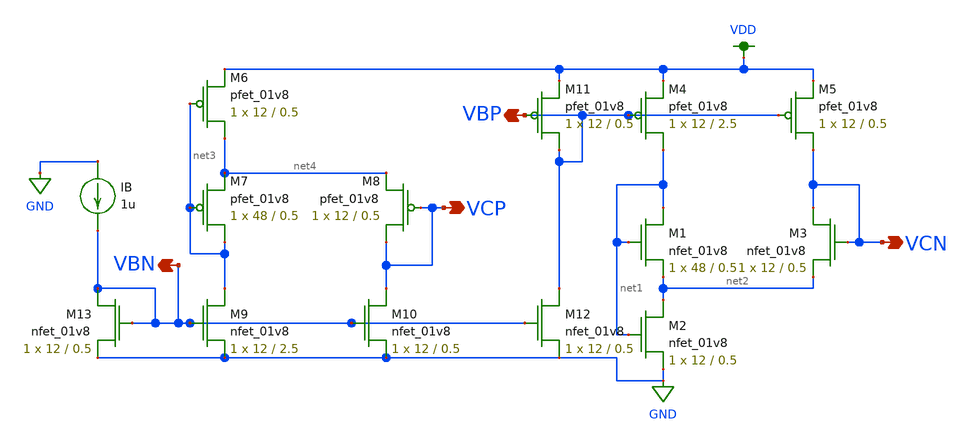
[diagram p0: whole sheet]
** sch_path: MP3/BiasGen (copy).sch
**.subckt BiasGen (copy) VCN VCP VBP VBN
*.opin VCN
*.opin VCP
*.opin VBP
*.opin VBN
XM1 net1 net1 net2 GND sky130_fd_pr__nfet_01v8 L=0.5 W=48 nf=1 ad='int((nf+1)/2) * W/nf * 0.29' as='int((nf+2)/2) * W/nf * 0.29'
+ pd='2*int((nf+1)/2) * (W/nf + 0.29)' ps='2*int((nf+2)/2) * (W/nf + 0.29)' nrd='0.29 / W' nrs='0.29 / W'
+ sa=0 sb=0 sd=0 mult=1 m=1
XM2 net2 net1 GND GND sky130_fd_pr__nfet_01v8 L=0.5 W=12 nf=1 ad='int((nf+1)/2) * W/nf * 0.29' as='int((nf+2)/2) * W/nf * 0.29'
+ pd='2*int((nf+1)/2) * (W/nf + 0.29)' ps='2*int((nf+2)/2) * (W/nf + 0.29)' nrd='0.29 / W' nrs='0.29 / W'
+ sa=0 sb=0 sd=0 mult=1 m=1
XM3 VCN VCN net2 GND sky130_fd_pr__nfet_01v8 L=0.5 W=12 nf=1 ad='int((nf+1)/2) * W/nf * 0.29' as='int((nf+2)/2) * W/nf * 0.29'
+ pd='2*int((nf+1)/2) * (W/nf + 0.29)' ps='2*int((nf+2)/2) * (W/nf + 0.29)' nrd='0.29 / W' nrs='0.29 / W'
+ sa=0 sb=0 sd=0 mult=1 m=1
XM4 net1 VBP VDD VDD sky130_fd_pr__pfet_01v8 L=2.5 W=12 nf=1 ad='int((nf+1)/2) * W/nf * 0.29' as='int((nf+2)/2) * W/nf * 0.29'
+ pd='2*int((nf+1)/2) * (W/nf + 0.29)' ps='2*int((nf+2)/2) * (W/nf + 0.29)' nrd='0.29 / W' nrs='0.29 / W'
+ sa=0 sb=0 sd=0 mult=1 m=1
XM5 VCN VBP VDD VDD sky130_fd_pr__pfet_01v8 L=0.5 W=12 nf=1 ad='int((nf+1)/2) * W/nf * 0.29' as='int((nf+2)/2) * W/nf * 0.29'
+ pd='2*int((nf+1)/2) * (W/nf + 0.29)' ps='2*int((nf+2)/2) * (W/nf + 0.29)' nrd='0.29 / W' nrs='0.29 / W'
+ sa=0 sb=0 sd=0 mult=1 m=1
XM6 net4 net3 VDD VDD sky130_fd_pr__pfet_01v8 L=0.5 W=12 nf=1 ad='int((nf+1)/2) * W/nf * 0.29' as='int((nf+2)/2) * W/nf * 0.29'
+ pd='2*int((nf+1)/2) * (W/nf + 0.29)' ps='2*int((nf+2)/2) * (W/nf + 0.29)' nrd='0.29 / W' nrs='0.29 / W'
+ sa=0 sb=0 sd=0 mult=1 m=1
XM7 net3 net3 net4 VDD sky130_fd_pr__pfet_01v8 L=0.5 W=48 nf=1 ad='int((nf+1)/2) * W/nf * 0.29' as='int((nf+2)/2) * W/nf * 0.29'
+ pd='2*int((nf+1)/2) * (W/nf + 0.29)' ps='2*int((nf+2)/2) * (W/nf + 0.29)' nrd='0.29 / W' nrs='0.29 / W'
+ sa=0 sb=0 sd=0 mult=1 m=1
XM8 VCP VCP net4 VDD sky130_fd_pr__pfet_01v8 L=0.5 W=12 nf=1 ad='int((nf+1)/2) * W/nf * 0.29' as='int((nf+2)/2) * W/nf * 0.29'
+ pd='2*int((nf+1)/2) * (W/nf + 0.29)' ps='2*int((nf+2)/2) * (W/nf + 0.29)' nrd='0.29 / W' nrs='0.29 / W'
+ sa=0 sb=0 sd=0 mult=1 m=1
XM9 net3 VBN GND GND sky130_fd_pr__nfet_01v8 L=2.5 W=12 nf=1 ad='int((nf+1)/2) * W/nf * 0.29' as='int((nf+2)/2) * W/nf * 0.29'
+ pd='2*int((nf+1)/2) * (W/nf + 0.29)' ps='2*int((nf+2)/2) * (W/nf + 0.29)' nrd='0.29 / W' nrs='0.29 / W'
+ sa=0 sb=0 sd=0 mult=1 m=1
XM10 VCP VBN GND GND sky130_fd_pr__nfet_01v8 L=0.5 W=12 nf=1 ad='int((nf+1)/2) * W/nf * 0.29' as='int((nf+2)/2) * W/nf * 0.29'
+ pd='2*int((nf+1)/2) * (W/nf + 0.29)' ps='2*int((nf+2)/2) * (W/nf + 0.29)' nrd='0.29 / W' nrs='0.29 / W'
+ sa=0 sb=0 sd=0 mult=1 m=1
XM11 VBP VBP VDD VDD sky130_fd_pr__pfet_01v8 L=0.5 W=12 nf=1 ad='int((nf+1)/2) * W/nf * 0.29' as='int((nf+2)/2) * W/nf * 0.29'
+ pd='2*int((nf+1)/2) * (W/nf + 0.29)' ps='2*int((nf+2)/2) * (W/nf + 0.29)' nrd='0.29 / W' nrs='0.29 / W'
+ sa=0 sb=0 sd=0 mult=1 m=1
XM12 VBP VBN GND GND sky130_fd_pr__nfet_01v8 L=0.5 W=12 nf=1 ad='int((nf+1)/2) * W/nf * 0.29' as='int((nf+2)/2) * W/nf * 0.29'
+ pd='2*int((nf+1)/2) * (W/nf + 0.29)' ps='2*int((nf+2)/2) * (W/nf + 0.29)' nrd='0.29 / W' nrs='0.29 / W'
+ sa=0 sb=0 sd=0 mult=1 m=1
XM13 VBN VBN GND GND sky130_fd_pr__nfet_01v8 L=0.5 W=12 nf=1 ad='int((nf+1)/2) * W/nf * 0.29' as='int((nf+2)/2) * W/nf * 0.29'
+ pd='2*int((nf+1)/2) * (W/nf + 0.29)' ps='2*int((nf+2)/2) * (W/nf + 0.29)' nrd='0.29 / W' nrs='0.29 / W'
+ sa=0 sb=0 sd=0 mult=1 m=1
IB GND VBN 1u
**.ends
.GLOBAL VDD
.GLOBAL GND
.end
